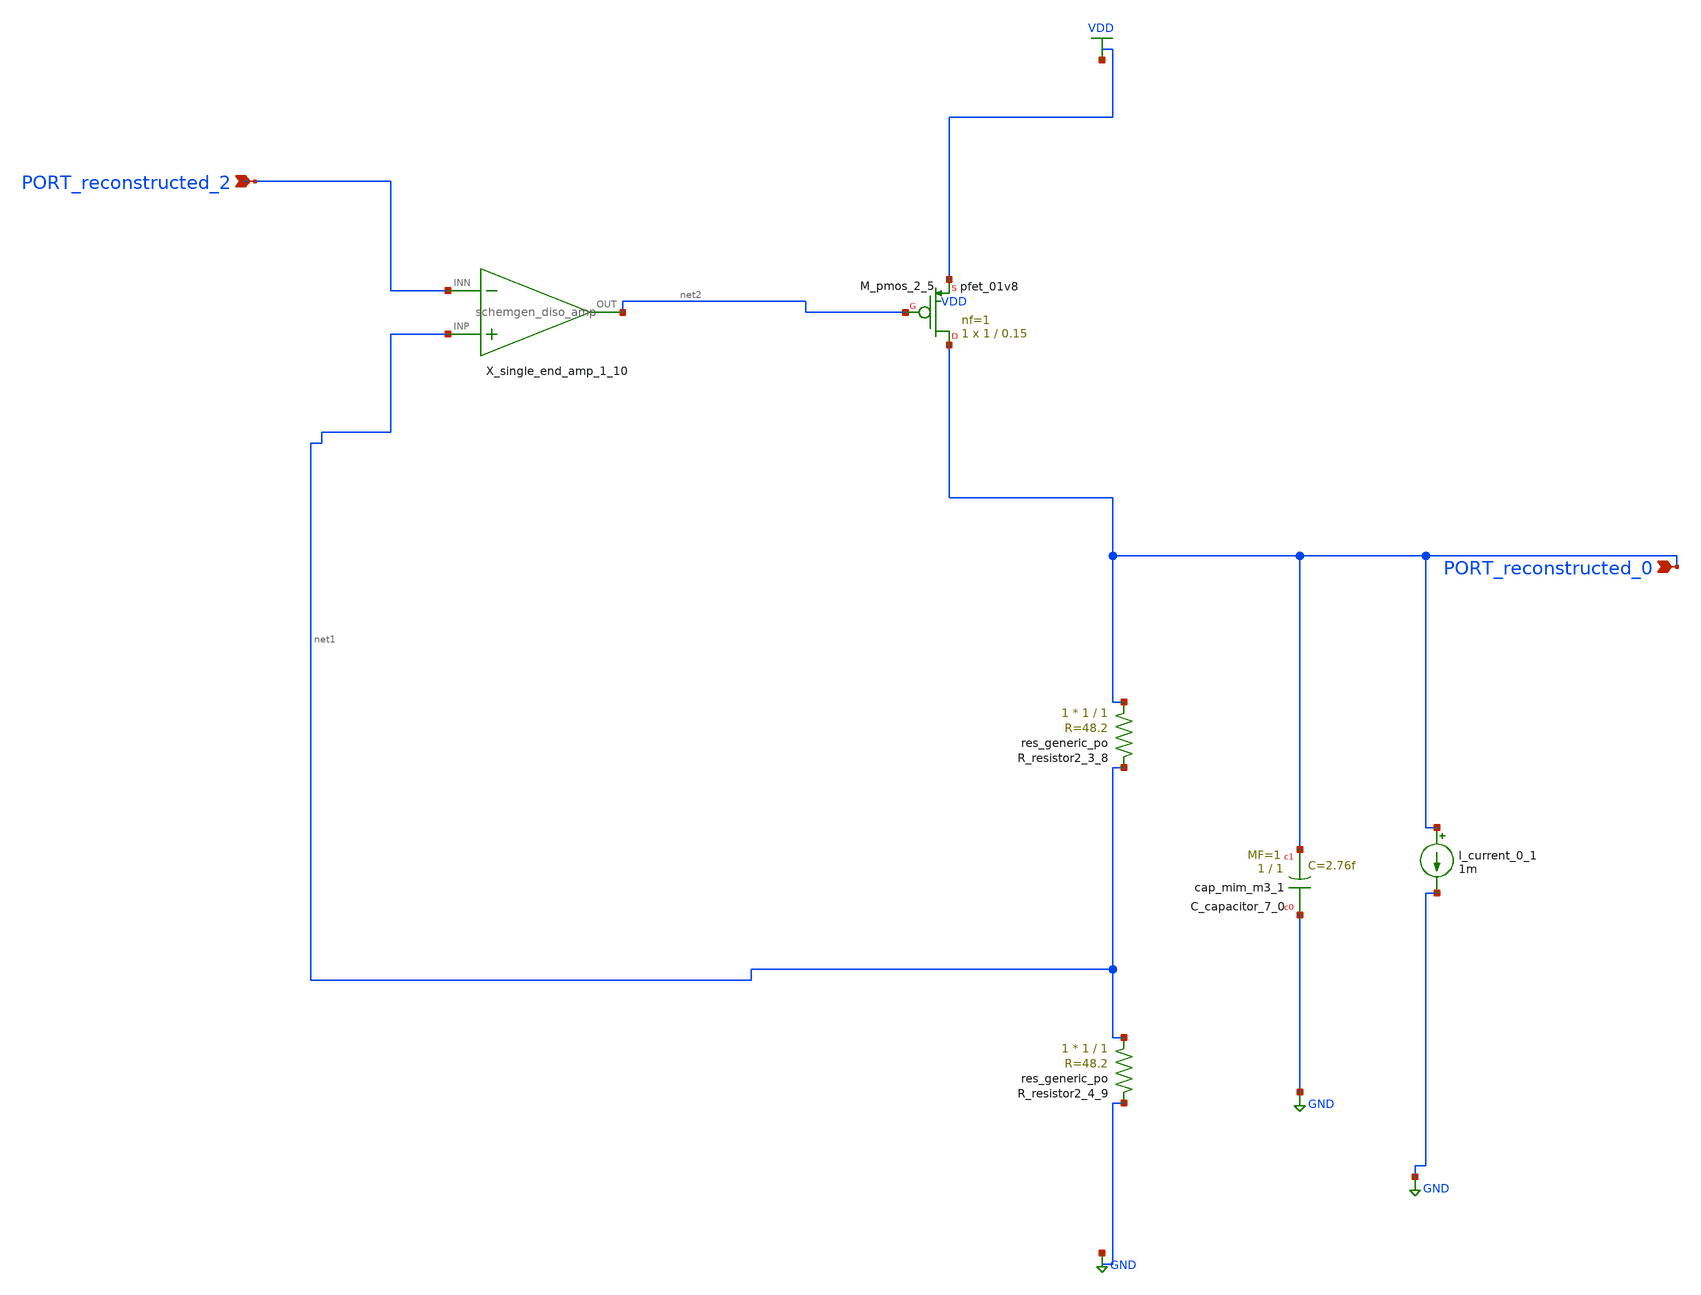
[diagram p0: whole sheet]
** sch_path: schematics/Image2Net/058.sch
**.subckt 058 PORT_reconstructed_0 PORT_reconstructed_2
*.ipin PORT_reconstructed_0
*.ipin PORT_reconstructed_2
XC_capacitor_7_0 GND PORT_reconstructed_0 sky130_fd_pr__cap_mim_m3_1 W=1 L=1 MF=1 m=1
I_current_0_1 PORT_reconstructed_0 GND 1m
XM_pmos_2_5 PORT_reconstructed_0 net2 VDD VDD sky130_fd_pr__pfet_01v8 L=0.15 W=1 nf=1 ad='int((1 + 1)/2) * 1 / 1 * 0.29'
+ as='int((1 + 2)/2) * 1 / 1 * 0.29' pd='2*int((1 + 1)/2) * (1 / 1 + 0.29)' ps='2*int((1 + 2)/2) * (1 / 1 + 0.29)'
+ nrd='0.29 / 1 ' nrs='0.29 / 1 ' sa=0 sb=0 sd=0 mult=1 m=1
XR_resistor2_3_8 PORT_reconstructed_0 net1 sky130_fd_pr__res_generic_po W=1 L=1 m=1
XR_resistor2_4_9 net1 GND sky130_fd_pr__res_generic_po W=1 L=1 m=1
X_single_end_amp_1_10 net1 PORT_reconstructed_2 net2 schemgen_diso_amp
**.ends

* expanding   symbol:  schemgen_diso_amp.sym # of pins=3
** sym_path: symbols/schemgen_diso_amp.sym
.subckt schemgen_diso_amp INP INN OUT
* SchemGen ideal op-amp: Vout = 1e5 * (V(INP) - V(INN))
E1 OUT 0 INP INN 1e5
.ends schemgen_diso_amp
.GLOBAL GND
.GLOBAL VDD
.end
